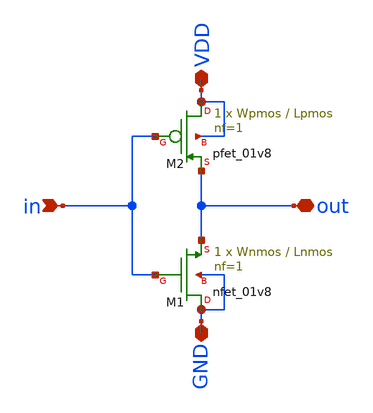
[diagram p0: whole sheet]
** sch_path: xschem/inv/inv_sparse_decoder2.sch
**.subckt inv_sparse_decoder2 in out VDD GND
*.ipin in
*.iopin out
*.iopin VDD
*.iopin GND
XM1 GND in out GND sky130_fd_pr__nfet_01v8 L=Lnmos W=Wnmos nf=1 ad='int((nf+1)/2) * W/nf * 0.29' as='int((nf+2)/2) * W/nf * 0.29'
+ pd='2*int((nf+1)/2) * (W/nf + 0.29)' ps='2*int((nf+2)/2) * (W/nf + 0.29)' nrd='0.29 / W' nrs='0.29 / W'
+ sa=0 sb=0 sd=0 mult=1 m=1
XM2 VDD in out VDD sky130_fd_pr__pfet_01v8 L=Lpmos W=Wpmos nf=1 ad='int((nf+1)/2) * W/nf * 0.29' as='int((nf+2)/2) * W/nf * 0.29'
+ pd='2*int((nf+1)/2) * (W/nf + 0.29)' ps='2*int((nf+2)/2) * (W/nf + 0.29)' nrd='0.29 / W' nrs='0.29 / W'
+ sa=0 sb=0 sd=0 mult=1 m=1
**.ends
.end
